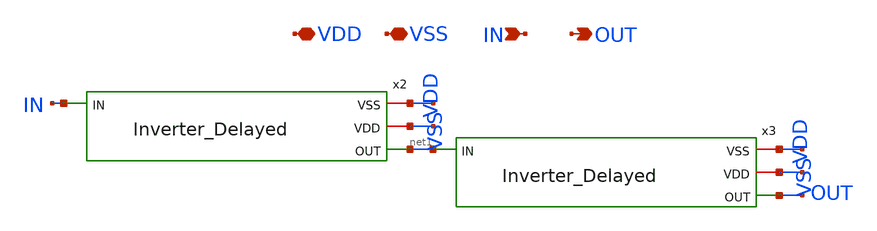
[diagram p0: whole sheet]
** sch_path: Clock_Generator_PAKISTAN_02/Schematics/Buffer_Delayed.sch
**.subckt Buffer_Delayed VDD VSS IN OUT
*.iopin VDD
*.iopin VSS
*.ipin IN
*.opin OUT
x2 VSS VDD net1 IN Inverter_Delayed
x3 VSS VDD OUT net1 Inverter_Delayed
**.ends
.end
